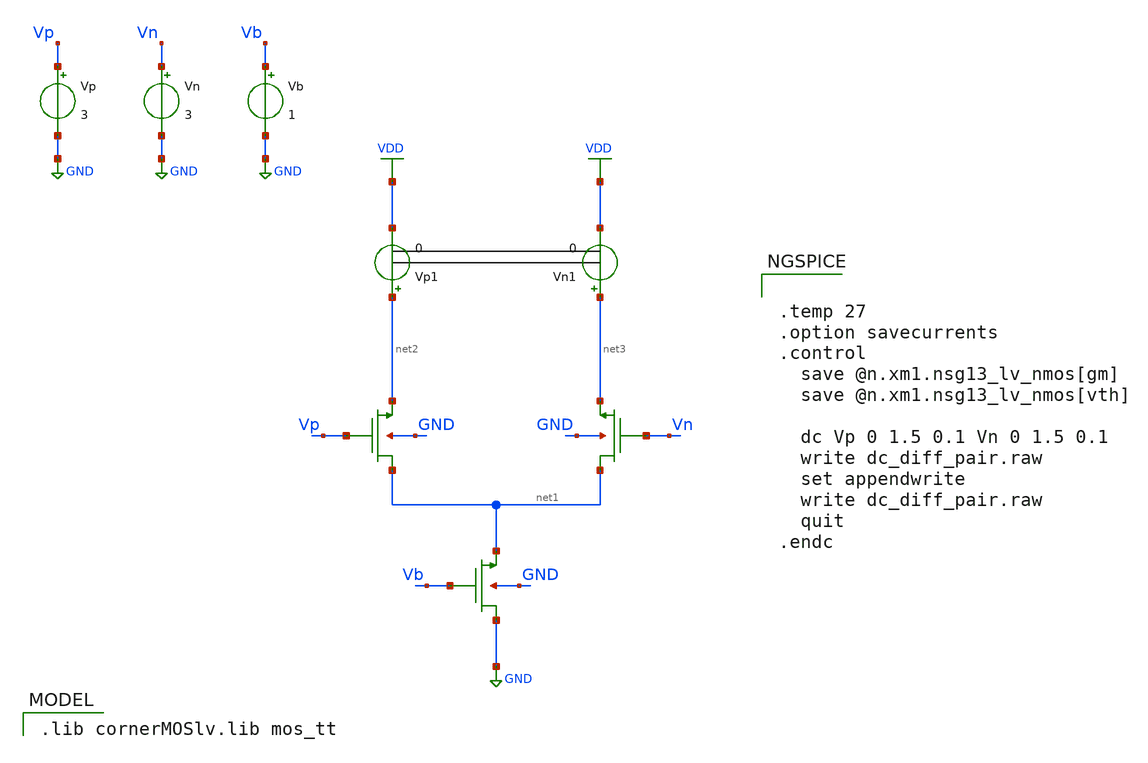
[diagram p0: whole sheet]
** sch_path: CKT_8/xschem/circuit.sch
**.subckt circuit
XM1 net1 Vp net2 GND sg13_lv_nmos w=1.0u l=0.45u ng=1 m=1 mm_ok=1
XM2 net1 Vn net3 GND sg13_lv_nmos w=1.0u l=0.45u ng=1 m=1 mm_ok=1
XM3 GND Vb net1 GND sg13_lv_nmos w=1.0u l=0.45u ng=1 m=1 mm_ok=1
Vp Vp GND 3
.save i(vp)
Vn Vn GND 3
.save i(vn)
Vb Vb GND 1
.save i(vb)
Vp1 net2 VDD 0
.save i(vp1)
Vn1 net3 VDD 0
.save i(vn1)
**** begin user architecture code
 .lib cornerMOSlv.lib mos_tt



.temp 27
.option savecurrents
.control
  save @n.xm1.nsg13_lv_nmos[gm]
  save @n.xm1.nsg13_lv_nmos[vth]

  dc Vp 0 1.5 0.1 Vn 0 1.5 0.1
  write dc_diff_pair.raw
  set appendwrite
  write dc_diff_pair.raw
  quit
.endc


**** end user architecture code
**.ends
.GLOBAL GND
.GLOBAL VDD
.end
